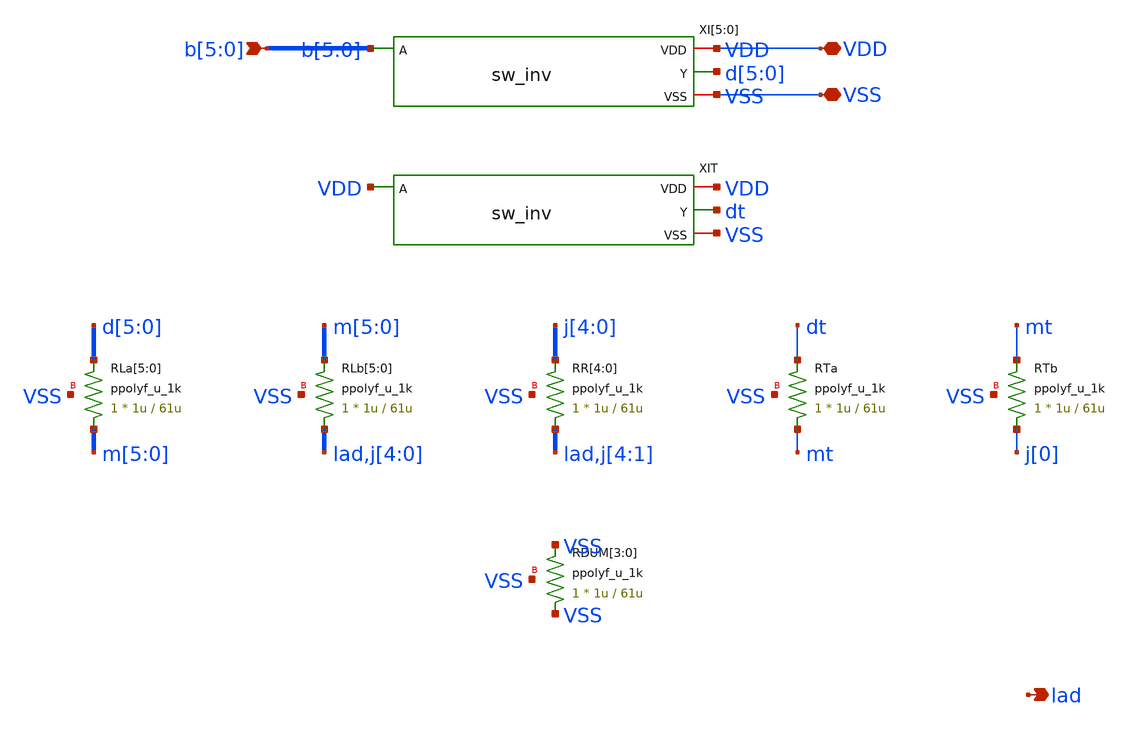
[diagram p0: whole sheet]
** sch_path: xschem/pll_dac/schr2r6.sch
**.subckt schr2r6 VDD VSS b[5],b[4],b[3],b[2],b[1],b[0] lad
*.iopin VDD
*.iopin VSS
*.ipin b[5],b[4],b[3],b[2],b[1],b[0]
*.opin lad
XI[5] VDD b[5] d[5] VSS sw_inv
XI[4] VDD b[4] d[4] VSS sw_inv
XI[3] VDD b[3] d[3] VSS sw_inv
XI[2] VDD b[2] d[2] VSS sw_inv
XI[1] VDD b[1] d[1] VSS sw_inv
XI[0] VDD b[0] d[0] VSS sw_inv
XIT VDD VDD dt VSS sw_inv
XRLa[5] m[5] d[5] VSS ppolyf_u_1k r_width=1u r_length=61u m=1
XRLa[4] m[4] d[4] VSS ppolyf_u_1k r_width=1u r_length=61u m=1
XRLa[3] m[3] d[3] VSS ppolyf_u_1k r_width=1u r_length=61u m=1
XRLa[2] m[2] d[2] VSS ppolyf_u_1k r_width=1u r_length=61u m=1
XRLa[1] m[1] d[1] VSS ppolyf_u_1k r_width=1u r_length=61u m=1
XRLa[0] m[0] d[0] VSS ppolyf_u_1k r_width=1u r_length=61u m=1
XRLb[5] lad m[5] VSS ppolyf_u_1k r_width=1u r_length=61u m=1
XRLb[4] j[4] m[4] VSS ppolyf_u_1k r_width=1u r_length=61u m=1
XRLb[3] j[3] m[3] VSS ppolyf_u_1k r_width=1u r_length=61u m=1
XRLb[2] j[2] m[2] VSS ppolyf_u_1k r_width=1u r_length=61u m=1
XRLb[1] j[1] m[1] VSS ppolyf_u_1k r_width=1u r_length=61u m=1
XRLb[0] j[0] m[0] VSS ppolyf_u_1k r_width=1u r_length=61u m=1
XRR[4] lad j[4] VSS ppolyf_u_1k r_width=1u r_length=61u m=1
XRR[3] j[4] j[3] VSS ppolyf_u_1k r_width=1u r_length=61u m=1
XRR[2] j[3] j[2] VSS ppolyf_u_1k r_width=1u r_length=61u m=1
XRR[1] j[2] j[1] VSS ppolyf_u_1k r_width=1u r_length=61u m=1
XRR[0] j[1] j[0] VSS ppolyf_u_1k r_width=1u r_length=61u m=1
XRTa mt dt VSS ppolyf_u_1k r_width=1u r_length=61u m=1
XRTb j[0] mt VSS ppolyf_u_1k r_width=1u r_length=61u m=1
XRDUM[3] VSS VSS VSS ppolyf_u_1k r_width=1u r_length=61u m=1
XRDUM[2] VSS VSS VSS ppolyf_u_1k r_width=1u r_length=61u m=1
XRDUM[1] VSS VSS VSS ppolyf_u_1k r_width=1u r_length=61u m=1
XRDUM[0] VSS VSS VSS ppolyf_u_1k r_width=1u r_length=61u m=1
**.ends

* expanding   symbol:  pll_dac/sw_inv.sym # of pins=4
** sym_path: xschem/pll_dac/sw_inv.sym
** sch_path: xschem/pll_dac/sw_inv.sch
.subckt sw_inv VDD A Y VSS
*.ipin A
*.iopin VDD
*.iopin VSS
*.opin Y
XM1 Y A VSS VSS nfet_03v3 L=0.28u W=2u nf=1 ad='int((nf+1)/2) * W/nf * 0.18u' as='int((nf+2)/2) * W/nf * 0.18u'
+ pd='2*int((nf+1)/2) * (W/nf + 0.18u)' ps='2*int((nf+2)/2) * (W/nf + 0.18u)' nrd='0.18u / W' nrs='0.18u / W'
+ sa=0 sb=0 sd=0 m=1
XM2 Y A VDD VDD pfet_03v3 L=0.28u W=5.6u nf=1 ad='int((nf+1)/2) * W/nf * 0.18u' as='int((nf+2)/2) * W/nf * 0.18u'
+ pd='2*int((nf+1)/2) * (W/nf + 0.18u)' ps='2*int((nf+2)/2) * (W/nf + 0.18u)' nrd='0.18u / W' nrs='0.18u / W'
+ sa=0 sb=0 sd=0 m=1
.ends

.end
